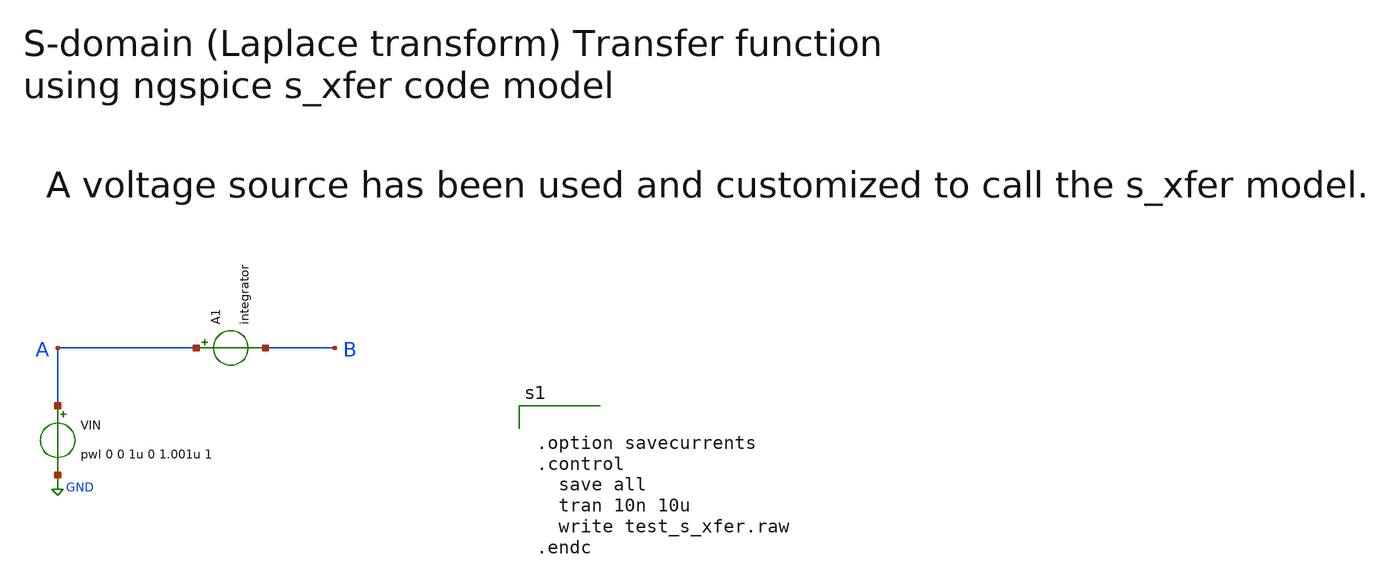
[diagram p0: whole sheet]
** sch_path: sky130A/xschem_libs/sky130_tests/test_s_xfer/schematic/test_s_xfer.sch
* Copyright 2021 Stefan Frederik Schippers
* Licensed under the Apache License, Version 2.0 (the "License");
* you may not use this file except in compliance with the License.
* You may obtain a copy of the License at
* https://www.apache.org/licenses/LICENSE-2.0
* Unless required by applicable law or agreed to in writing, software
* distributed under the License is distributed on an "AS IS" BASIS,
* WITHOUT WARRANTIES OR CONDITIONS OF ANY KIND, either express or implied.
* See the License for the specific language governing permissions and
* limitations under the License.
**.subckt test_s_xfer
A1 A B integrator
VIN A GND pwl 0 0 1u 0 1.001u 1
**** begin user architecture code


.option savecurrents
.control
  save all
  tran 10n 10u
  write test_s_xfer.raw
.endc

**** end user architecture code
**.ends
.GLOBAL GND
**** begin user architecture code

.model integrator s_xfer(num_coeff=[1] den_coeff=[1 0] int_ic=[0] denormalized_freq=1e5)

**** end user architecture code
.end
